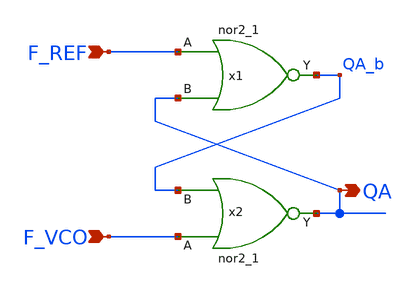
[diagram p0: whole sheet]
** sch_path: projects/pll/pfd/xschem_ngspice/phase_frequency_detector_3.sch
**.subckt phase_frequency_detector_3 F_REF QA F_VCO
*.ipin F_REF
*.opin QA
*.ipin F_VCO
x1 F_REF QA VGND VSUBS VPB VPWR QA_b sky130_fd_sc_hd__nor2_1
x2 F_VCO QA_b VGND VSUBS VPB VPWR QA sky130_fd_sc_hd__nor2_1
**.ends
.end
